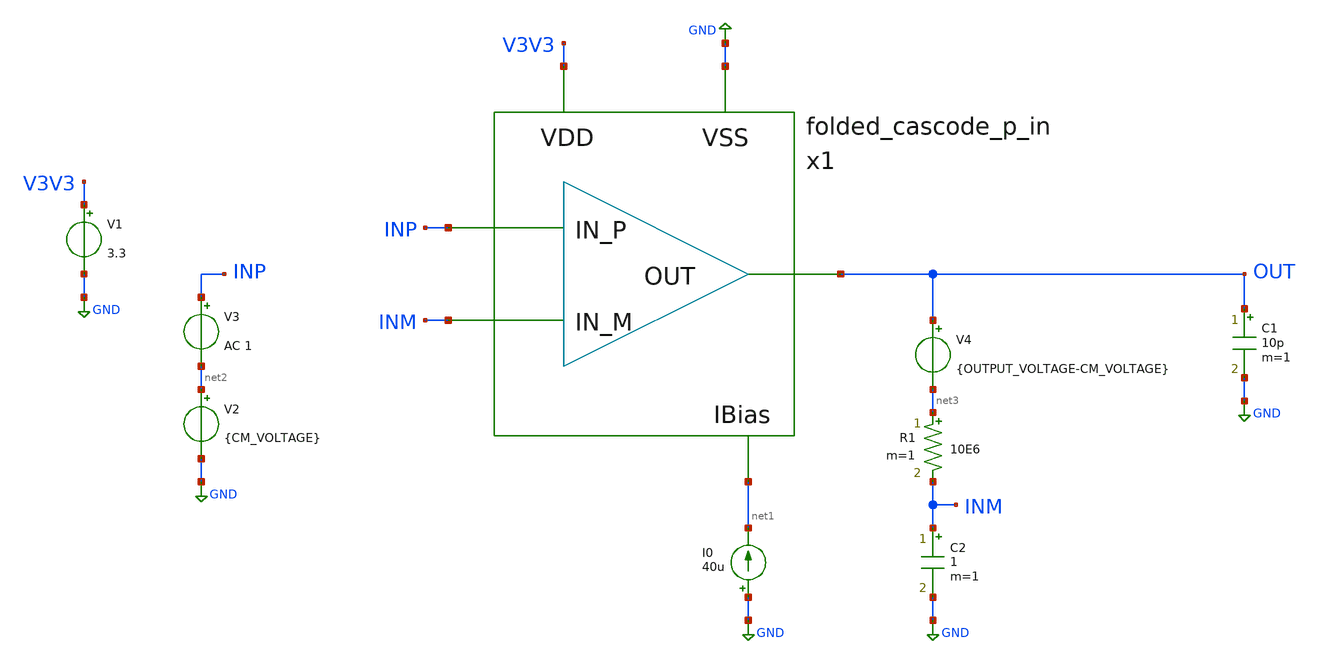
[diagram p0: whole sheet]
** sch_path: design/folded-cascode-p-in/folded_cascode_p_in_tb.sch
**.subckt folded_cascode_p_in_tb
x1 INP INM OUT V3V3 GND net1 folded_cascode_p_in
V1 V3V3 GND 3.3
I0 GND net1 40u
V2 net2 GND {CM_VOLTAGE}
V3 INP net2 AC 1
C1 OUT GND 10p m=1
R1 net3 INM 10E6 m=1
V4 OUT net3 {OUTPUT_VOLTAGE-CM_VOLTAGE}
C2 INM GND 1 m=1
**** begin user architecture code

.include $::SKYWATER_MODELS/cells/nfet_01v8/sky130_fd_pr__nfet_01v8__tt.corner.spice
.include $::SKYWATER_MODELS/cells/nfet_01v8_lvt/sky130_fd_pr__nfet_01v8_lvt__tt.corner.spice
.include $::SKYWATER_MODELS/cells/pfet_01v8/sky130_fd_pr__pfet_01v8__tt.corner.spice
.include $::SKYWATER_MODELS/cells/nfet_03v3_nvt/sky130_fd_pr__nfet_03v3_nvt__tt.corner.spice
.include $::SKYWATER_MODELS/cells/nfet_05v0_nvt/sky130_fd_pr__nfet_05v0_nvt__tt.corner.spice
.include $::SKYWATER_MODELS/cells/esd_nfet_01v8/sky130_fd_pr__esd_nfet_01v8__tt.corner.spice
.include $::SKYWATER_MODELS/cells/pfet_01v8_lvt/sky130_fd_pr__pfet_01v8_lvt__tt.corner.spice
.include $::SKYWATER_MODELS/cells/pfet_01v8_hvt/sky130_fd_pr__pfet_01v8_hvt__tt.corner.spice
.include $::SKYWATER_MODELS/cells/esd_pfet_g5v0d10v5/sky130_fd_pr__esd_pfet_g5v0d10v5__tt.corner.spice
.include $::SKYWATER_MODELS/cells/pfet_g5v0d10v5/sky130_fd_pr__pfet_g5v0d10v5__tt.corner.spice
.include $::SKYWATER_MODELS/cells/pfet_g5v0d16v0/sky130_fd_pr__pfet_g5v0d16v0__tt.corner.spice
.include $::SKYWATER_MODELS/cells/nfet_g5v0d10v5/sky130_fd_pr__nfet_g5v0d10v5__tt.corner.spice
.include $::SKYWATER_MODELS/cells/nfet_g5v0d16v0/sky130_fd_pr__nfet_g5v0d16v0__tt_discrete.corner.spice
.include $::SKYWATER_MODELS/cells/esd_nfet_g5v0d10v5/sky130_fd_pr__esd_nfet_g5v0d10v5__tt.corner.spice
.include $::SKYWATER_MODELS/models/corners/tt/nonfet.spice
* Mismatch parameters
.include $::SKYWATER_MODELS/cells/nfet_01v8/sky130_fd_pr__nfet_01v8__mismatch.corner.spice
.include $::SKYWATER_MODELS/cells/pfet_01v8/sky130_fd_pr__pfet_01v8__mismatch.corner.spice
.include $::SKYWATER_MODELS/cells/nfet_01v8_lvt/sky130_fd_pr__nfet_01v8_lvt__mismatch.corner.spice
.include $::SKYWATER_MODELS/cells/pfet_01v8_lvt/sky130_fd_pr__pfet_01v8_lvt__mismatch.corner.spice
.include $::SKYWATER_MODELS/cells/pfet_01v8_hvt/sky130_fd_pr__pfet_01v8_hvt__mismatch.corner.spice
.include $::SKYWATER_MODELS/cells/nfet_g5v0d10v5/sky130_fd_pr__nfet_g5v0d10v5__mismatch.corner.spice
.include $::SKYWATER_MODELS/cells/pfet_g5v0d10v5/sky130_fd_pr__pfet_g5v0d10v5__mismatch.corner.spice
.include $::SKYWATER_MODELS/cells/nfet_05v0_nvt/sky130_fd_pr__nfet_05v0_nvt__mismatch.corner.spice
.include $::SKYWATER_MODELS/cells/nfet_03v3_nvt/sky130_fd_pr__nfet_03v3_nvt__mismatch.corner.spice
* Resistor$::SKYWATER_MODELS/Capacitor
.include $::SKYWATER_MODELS/models/r+c/res_typical__cap_typical.spice
.include $::SKYWATER_MODELS/models/r+c/res_typical__cap_typical__lin.spice
* Special cells
.include $::SKYWATER_MODELS/models/corners/tt/specialized_cells.spice
* All models
.include $::SKYWATER_MODELS/models/all.spice
* Corner
.include $::SKYWATER_MODELS/models/corners/tt/rf.spice



.param CM_VOLTAGE = 1.25
.param OUTPUT_VOLTAGE = 0.5
.control
save all
ac dec 200 10 1000Meg
settype decibel out
plot vdb(out)
let phase_val = 180/PI*cph(out)
let phase_margin_val = 180 + 180/PI*cph(out)
settype phase phase_val
plot phase_val
meas ac phase_margin find phase_margin_val when vdb(out)=0
meas ac crossover_freq WHEN vdb(out)=0
op
print v(inp)
print v(inm)
print v(out)
let v_offset = v(inp)-v(inm)
print v_offset
.endc


**** end user architecture code
**.ends

* expanding   symbol:  design/folded-cascode-p-in/folded_cascode_p_in.sym # of pins=6
** sym_path: design/folded-cascode-p-in/folded_cascode_p_in.sym
** sch_path: design/folded-cascode-p-in/folded_cascode_p_in.sch
.subckt folded_cascode_p_in IN_P IN_M OUT VDD VSS VBN
*.ipin IN_P
*.ipin IN_M
*.ipin OUT
*.ipin VDD
*.ipin VSS
*.ipin VBN
XM7 net4 VBP VDD VDD sky130_fd_pr__pfet_g5v0d10v5 L=1 W=5 nf=1 ad='int((nf+1)/2) * W/nf * 0.29' as='int((nf+2)/2) * W/nf * 0.29'
+ pd='2*int((nf+1)/2) * (W/nf + 0.29)' ps='2*int((nf+2)/2) * (W/nf + 0.29)' nrd='0.29 / W' nrs='0.29 / W'
+ sa=0 sb=0 sd=0 mult=12 m=12
XM8 VS1_P IN_M net4 VDD sky130_fd_pr__pfet_g5v0d10v5 L=1 W=5 nf=1 ad='int((nf+1)/2) * W/nf * 0.29' as='int((nf+2)/2) * W/nf * 0.29'
+ pd='2*int((nf+1)/2) * (W/nf + 0.29)' ps='2*int((nf+2)/2) * (W/nf + 0.29)' nrd='0.29 / W' nrs='0.29 / W'
+ sa=0 sb=0 sd=0 mult=24 m=24
XM15 VS1_M IN_P net4 VDD sky130_fd_pr__pfet_g5v0d10v5 L=1 W=5 nf=1 ad='int((nf+1)/2) * W/nf * 0.29' as='int((nf+2)/2) * W/nf * 0.29'
+ pd='2*int((nf+1)/2) * (W/nf + 0.29)' ps='2*int((nf+2)/2) * (W/nf + 0.29)' nrd='0.29 / W' nrs='0.29 / W'
+ sa=0 sb=0 sd=0 mult=24 m=24
XM16 VS1_P VBN_INT VSS VSS sky130_fd_pr__nfet_g5v0d10v5 L=1 W=5 nf=1 ad='int((nf+1)/2) * W/nf * 0.29'
+ as='int((nf+2)/2) * W/nf * 0.29' pd='2*int((nf+1)/2) * (W/nf + 0.29)' ps='2*int((nf+2)/2) * (W/nf + 0.29)'
+ nrd='0.29 / W' nrs='0.29 / W' sa=0 sb=0 sd=0 mult=10 m=10
XM20 VS1_M VBN_INT VSS VSS sky130_fd_pr__nfet_g5v0d10v5 L=1 W=5 nf=1 ad='int((nf+1)/2) * W/nf * 0.29'
+ as='int((nf+2)/2) * W/nf * 0.29' pd='2*int((nf+1)/2) * (W/nf + 0.29)' ps='2*int((nf+2)/2) * (W/nf + 0.29)'
+ nrd='0.29 / W' nrs='0.29 / W' sa=0 sb=0 sd=0 mult=10 m=10
XM22 net3 VCP net1 VDD sky130_fd_pr__pfet_g5v0d10v5 L=1 W=5 nf=1 ad='int((nf+1)/2) * W/nf * 0.29' as='int((nf+2)/2) * W/nf * 0.29'
+ pd='2*int((nf+1)/2) * (W/nf + 0.29)' ps='2*int((nf+2)/2) * (W/nf + 0.29)' nrd='0.29 / W' nrs='0.29 / W'
+ sa=0 sb=0 sd=0 mult=4 m=4
XM23 net1 net3 VDD VDD sky130_fd_pr__pfet_g5v0d10v5 L=1 W=5 nf=1 ad='int((nf+1)/2) * W/nf * 0.29' as='int((nf+2)/2) * W/nf * 0.29'
+ pd='2*int((nf+1)/2) * (W/nf + 0.29)' ps='2*int((nf+2)/2) * (W/nf + 0.29)' nrd='0.29 / W' nrs='0.29 / W'
+ sa=0 sb=0 sd=0 mult=4 m=4
XM24 OUT VCP net2 VDD sky130_fd_pr__pfet_g5v0d10v5 L=1 W=5 nf=1 ad='int((nf+1)/2) * W/nf * 0.29' as='int((nf+2)/2) * W/nf * 0.29'
+ pd='2*int((nf+1)/2) * (W/nf + 0.29)' ps='2*int((nf+2)/2) * (W/nf + 0.29)' nrd='0.29 / W' nrs='0.29 / W'
+ sa=0 sb=0 sd=0 mult=4 m=4
XM25 net2 net3 VDD VDD sky130_fd_pr__pfet_g5v0d10v5 L=1 W=5 nf=1 ad='int((nf+1)/2) * W/nf * 0.29' as='int((nf+2)/2) * W/nf * 0.29'
+ pd='2*int((nf+1)/2) * (W/nf + 0.29)' ps='2*int((nf+2)/2) * (W/nf + 0.29)' nrd='0.29 / W' nrs='0.29 / W'
+ sa=0 sb=0 sd=0 mult=4 m=4
XM26 OUT VCN VS1_P VSS sky130_fd_pr__nfet_g5v0d10v5 L=1 W=5 nf=1 ad='int((nf+1)/2) * W/nf * 0.29' as='int((nf+2)/2) * W/nf * 0.29'
+ pd='2*int((nf+1)/2) * (W/nf + 0.29)' ps='2*int((nf+2)/2) * (W/nf + 0.29)' nrd='0.29 / W' nrs='0.29 / W'
+ sa=0 sb=0 sd=0 mult=4 m=4
XM27 net3 VCN VS1_M VSS sky130_fd_pr__nfet_g5v0d10v5 L=1 W=5 nf=1 ad='int((nf+1)/2) * W/nf * 0.29' as='int((nf+2)/2) * W/nf * 0.29'
+ pd='2*int((nf+1)/2) * (W/nf + 0.29)' ps='2*int((nf+2)/2) * (W/nf + 0.29)' nrd='0.29 / W' nrs='0.29 / W'
+ sa=0 sb=0 sd=0 mult=4 m=4
XM29 VBN_INT VBN_INT VSS VSS sky130_fd_pr__nfet_g5v0d10v5 L=1 W=5 nf=1 ad='int((nf+1)/2) * W/nf * 0.29'
+ as='int((nf+2)/2) * W/nf * 0.29' pd='2*int((nf+1)/2) * (W/nf + 0.29)' ps='2*int((nf+2)/2) * (W/nf + 0.29)'
+ nrd='0.29 / W' nrs='0.29 / W' sa=0 sb=0 sd=0 mult=1 m=1
XM30 VBN_INT VBP VDD VDD sky130_fd_pr__pfet_g5v0d10v5 L=1 W=5 nf=1 ad='int((nf+1)/2) * W/nf * 0.29' as='int((nf+2)/2) * W/nf * 0.29'
+ pd='2*int((nf+1)/2) * (W/nf + 0.29)' ps='2*int((nf+2)/2) * (W/nf + 0.29)' nrd='0.29 / W' nrs='0.29 / W'
+ sa=0 sb=0 sd=0 mult=1 m=1
XM14 VBN_INT VBN_INT VS1_P VDD sky130_fd_pr__pfet_g5v0d10v5 L=1 W=5 nf=1 ad='int((nf+1)/2) * W/nf * 0.29'
+ as='int((nf+2)/2) * W/nf * 0.29' pd='2*int((nf+1)/2) * (W/nf + 0.29)' ps='2*int((nf+2)/2) * (W/nf + 0.29)'
+ nrd='0.29 / W' nrs='0.29 / W' sa=0 sb=0 sd=0 mult=1 m=1
XM17 VBN_INT VBN_INT VS1_M VDD sky130_fd_pr__pfet_g5v0d10v5 L=1 W=5 nf=1 ad='int((nf+1)/2) * W/nf * 0.29'
+ as='int((nf+2)/2) * W/nf * 0.29' pd='2*int((nf+1)/2) * (W/nf + 0.29)' ps='2*int((nf+2)/2) * (W/nf + 0.29)'
+ nrd='0.29 / W' nrs='0.29 / W' sa=0 sb=0 sd=0 mult=1 m=1
x1 VBN VCN VBP VCP VDD VSS cascode_bias
.ends


* expanding   symbol:  design/bias-circuit/cascode_bias.sym # of pins=6
** sym_path: design/bias-circuit/cascode_bias.sym
** sch_path: design/bias-circuit/cascode_bias.sch
.subckt cascode_bias VBN VCN VBP VCP VDD VSS
*.ipin VCN
*.ipin VBP
*.ipin VCP
*.ipin VDD
*.ipin VSS
*.ipin VBN
XM1 VBP VBP VDD VDD sky130_fd_pr__pfet_g5v0d10v5 L=1 W=5 nf=1 ad='int((nf+1)/2) * W/nf * 0.29' as='int((nf+2)/2) * W/nf * 0.29'
+ pd='2*int((nf+1)/2) * (W/nf + 0.29)' ps='2*int((nf+2)/2) * (W/nf + 0.29)' nrd='0.29 / W' nrs='0.29 / W'
+ sa=0 sb=0 sd=0 mult=1 m=1
XM2 net1 VBP net8 VDD sky130_fd_pr__pfet_g5v0d10v5 L=1 W=5 nf=1 ad='int((nf+1)/2) * W/nf * 0.29' as='int((nf+2)/2) * W/nf * 0.29'
+ pd='2*int((nf+1)/2) * (W/nf + 0.29)' ps='2*int((nf+2)/2) * (W/nf + 0.29)' nrd='0.29 / W' nrs='0.29 / W'
+ sa=0 sb=0 sd=0 mult=1 m=1
XM3 VCN VBP VDD VDD sky130_fd_pr__pfet_g5v0d10v5 L=1 W=5 nf=1 ad='int((nf+1)/2) * W/nf * 0.29' as='int((nf+2)/2) * W/nf * 0.29'
+ pd='2*int((nf+1)/2) * (W/nf + 0.29)' ps='2*int((nf+2)/2) * (W/nf + 0.29)' nrd='0.29 / W' nrs='0.29 / W'
+ sa=0 sb=0 sd=0 mult=1 m=1
XM4 net1 net1 net2 VSS sky130_fd_pr__nfet_g5v0d10v5 L=1 W=5 nf=1 ad='int((nf+1)/2) * W/nf * 0.29' as='int((nf+2)/2) * W/nf * 0.29'
+ pd='2*int((nf+1)/2) * (W/nf + 0.29)' ps='2*int((nf+2)/2) * (W/nf + 0.29)' nrd='0.29 / W' nrs='0.29 / W'
+ sa=0 sb=0 sd=0 mult=2 m=2
XM5 net2 net1 VSS VSS sky130_fd_pr__nfet_g5v0d10v5 L=1 W=5 nf=1 ad='int((nf+1)/2) * W/nf * 0.29' as='int((nf+2)/2) * W/nf * 0.29'
+ pd='2*int((nf+1)/2) * (W/nf + 0.29)' ps='2*int((nf+2)/2) * (W/nf + 0.29)' nrd='0.29 / W' nrs='0.29 / W'
+ sa=0 sb=0 sd=0 mult=1 m=1
XM21 VCN VCN net2 VSS sky130_fd_pr__nfet_g5v0d10v5 L=1 W=5 nf=1 ad='int((nf+1)/2) * W/nf * 0.29' as='int((nf+2)/2) * W/nf * 0.29'
+ pd='2*int((nf+1)/2) * (W/nf + 0.29)' ps='2*int((nf+2)/2) * (W/nf + 0.29)' nrd='0.29 / W' nrs='0.29 / W'
+ sa=0 sb=0 sd=0 mult=1 m=1
XM6 net3 VBN net6 VSS sky130_fd_pr__nfet_g5v0d10v5 L=1 W=5 nf=1 ad='int((nf+1)/2) * W/nf * 0.29' as='int((nf+2)/2) * W/nf * 0.29'
+ pd='2*int((nf+1)/2) * (W/nf + 0.29)' ps='2*int((nf+2)/2) * (W/nf + 0.29)' nrd='0.29 / W' nrs='0.29 / W'
+ sa=0 sb=0 sd=0 mult=1 m=1
XM9 VCP VBN VSS VSS sky130_fd_pr__nfet_g5v0d10v5 L=1 W=5 nf=1 ad='int((nf+1)/2) * W/nf * 0.29' as='int((nf+2)/2) * W/nf * 0.29'
+ pd='2*int((nf+1)/2) * (W/nf + 0.29)' ps='2*int((nf+2)/2) * (W/nf + 0.29)' nrd='0.29 / W' nrs='0.29 / W'
+ sa=0 sb=0 sd=0 mult=1 m=1
XM10 net3 net3 net4 VDD sky130_fd_pr__pfet_g5v0d10v5 L=1 W=5 nf=1 ad='int((nf+1)/2) * W/nf * 0.29' as='int((nf+2)/2) * W/nf * 0.29'
+ pd='2*int((nf+1)/2) * (W/nf + 0.29)' ps='2*int((nf+2)/2) * (W/nf + 0.29)' nrd='0.29 / W' nrs='0.29 / W'
+ sa=0 sb=0 sd=0 mult=2 m=2
XM11 VCP VCP net4 VDD sky130_fd_pr__pfet_g5v0d10v5 L=1 W=5 nf=1 ad='int((nf+1)/2) * W/nf * 0.29' as='int((nf+2)/2) * W/nf * 0.29'
+ pd='2*int((nf+1)/2) * (W/nf + 0.29)' ps='2*int((nf+2)/2) * (W/nf + 0.29)' nrd='0.29 / W' nrs='0.29 / W'
+ sa=0 sb=0 sd=0 mult=1 m=1
XM28 net4 net3 VDD VDD sky130_fd_pr__pfet_g5v0d10v5 L=1 W=5 nf=1 ad='int((nf+1)/2) * W/nf * 0.29' as='int((nf+2)/2) * W/nf * 0.29'
+ pd='2*int((nf+1)/2) * (W/nf + 0.29)' ps='2*int((nf+2)/2) * (W/nf + 0.29)' nrd='0.29 / W' nrs='0.29 / W'
+ sa=0 sb=0 sd=0 mult=1 m=1
XM12 VBP VBN VSS VSS sky130_fd_pr__nfet_g5v0d10v5 L=1 W=5 nf=1 ad='int((nf+1)/2) * W/nf * 0.29' as='int((nf+2)/2) * W/nf * 0.29'
+ pd='2*int((nf+1)/2) * (W/nf + 0.29)' ps='2*int((nf+2)/2) * (W/nf + 0.29)' nrd='0.29 / W' nrs='0.29 / W'
+ sa=0 sb=0 sd=0 mult=1 m=1
XM32 net8 VBP net5 VDD sky130_fd_pr__pfet_g5v0d10v5 L=1 W=5 nf=1 ad='int((nf+1)/2) * W/nf * 0.29' as='int((nf+2)/2) * W/nf * 0.29'
+ pd='2*int((nf+1)/2) * (W/nf + 0.29)' ps='2*int((nf+2)/2) * (W/nf + 0.29)' nrd='0.29 / W' nrs='0.29 / W'
+ sa=0 sb=0 sd=0 mult=1 m=1
XM33 net5 VBP VDD VDD sky130_fd_pr__pfet_g5v0d10v5 L=1 W=5 nf=1 ad='int((nf+1)/2) * W/nf * 0.29' as='int((nf+2)/2) * W/nf * 0.29'
+ pd='2*int((nf+1)/2) * (W/nf + 0.29)' ps='2*int((nf+2)/2) * (W/nf + 0.29)' nrd='0.29 / W' nrs='0.29 / W'
+ sa=0 sb=0 sd=0 mult=1 m=1
XM34 net6 VBN net7 VSS sky130_fd_pr__nfet_g5v0d10v5 L=1 W=5 nf=1 ad='int((nf+1)/2) * W/nf * 0.29' as='int((nf+2)/2) * W/nf * 0.29'
+ pd='2*int((nf+1)/2) * (W/nf + 0.29)' ps='2*int((nf+2)/2) * (W/nf + 0.29)' nrd='0.29 / W' nrs='0.29 / W'
+ sa=0 sb=0 sd=0 mult=1 m=1
XM35 net7 VBN VSS VSS sky130_fd_pr__nfet_g5v0d10v5 L=1 W=5 nf=1 ad='int((nf+1)/2) * W/nf * 0.29' as='int((nf+2)/2) * W/nf * 0.29'
+ pd='2*int((nf+1)/2) * (W/nf + 0.29)' ps='2*int((nf+2)/2) * (W/nf + 0.29)' nrd='0.29 / W' nrs='0.29 / W'
+ sa=0 sb=0 sd=0 mult=1 m=1
XM13 VBN VBN VSS VSS sky130_fd_pr__nfet_g5v0d10v5 L=1 W=5 nf=1 ad='int((nf+1)/2) * W/nf * 0.29' as='int((nf+2)/2) * W/nf * 0.29'
+ pd='2*int((nf+1)/2) * (W/nf + 0.29)' ps='2*int((nf+2)/2) * (W/nf + 0.29)' nrd='0.29 / W' nrs='0.29 / W'
+ sa=0 sb=0 sd=0 mult=1 m=1
.ends

.GLOBAL GND
**** begin user architecture code
[sky130_models]
**** end user architecture code
.end
